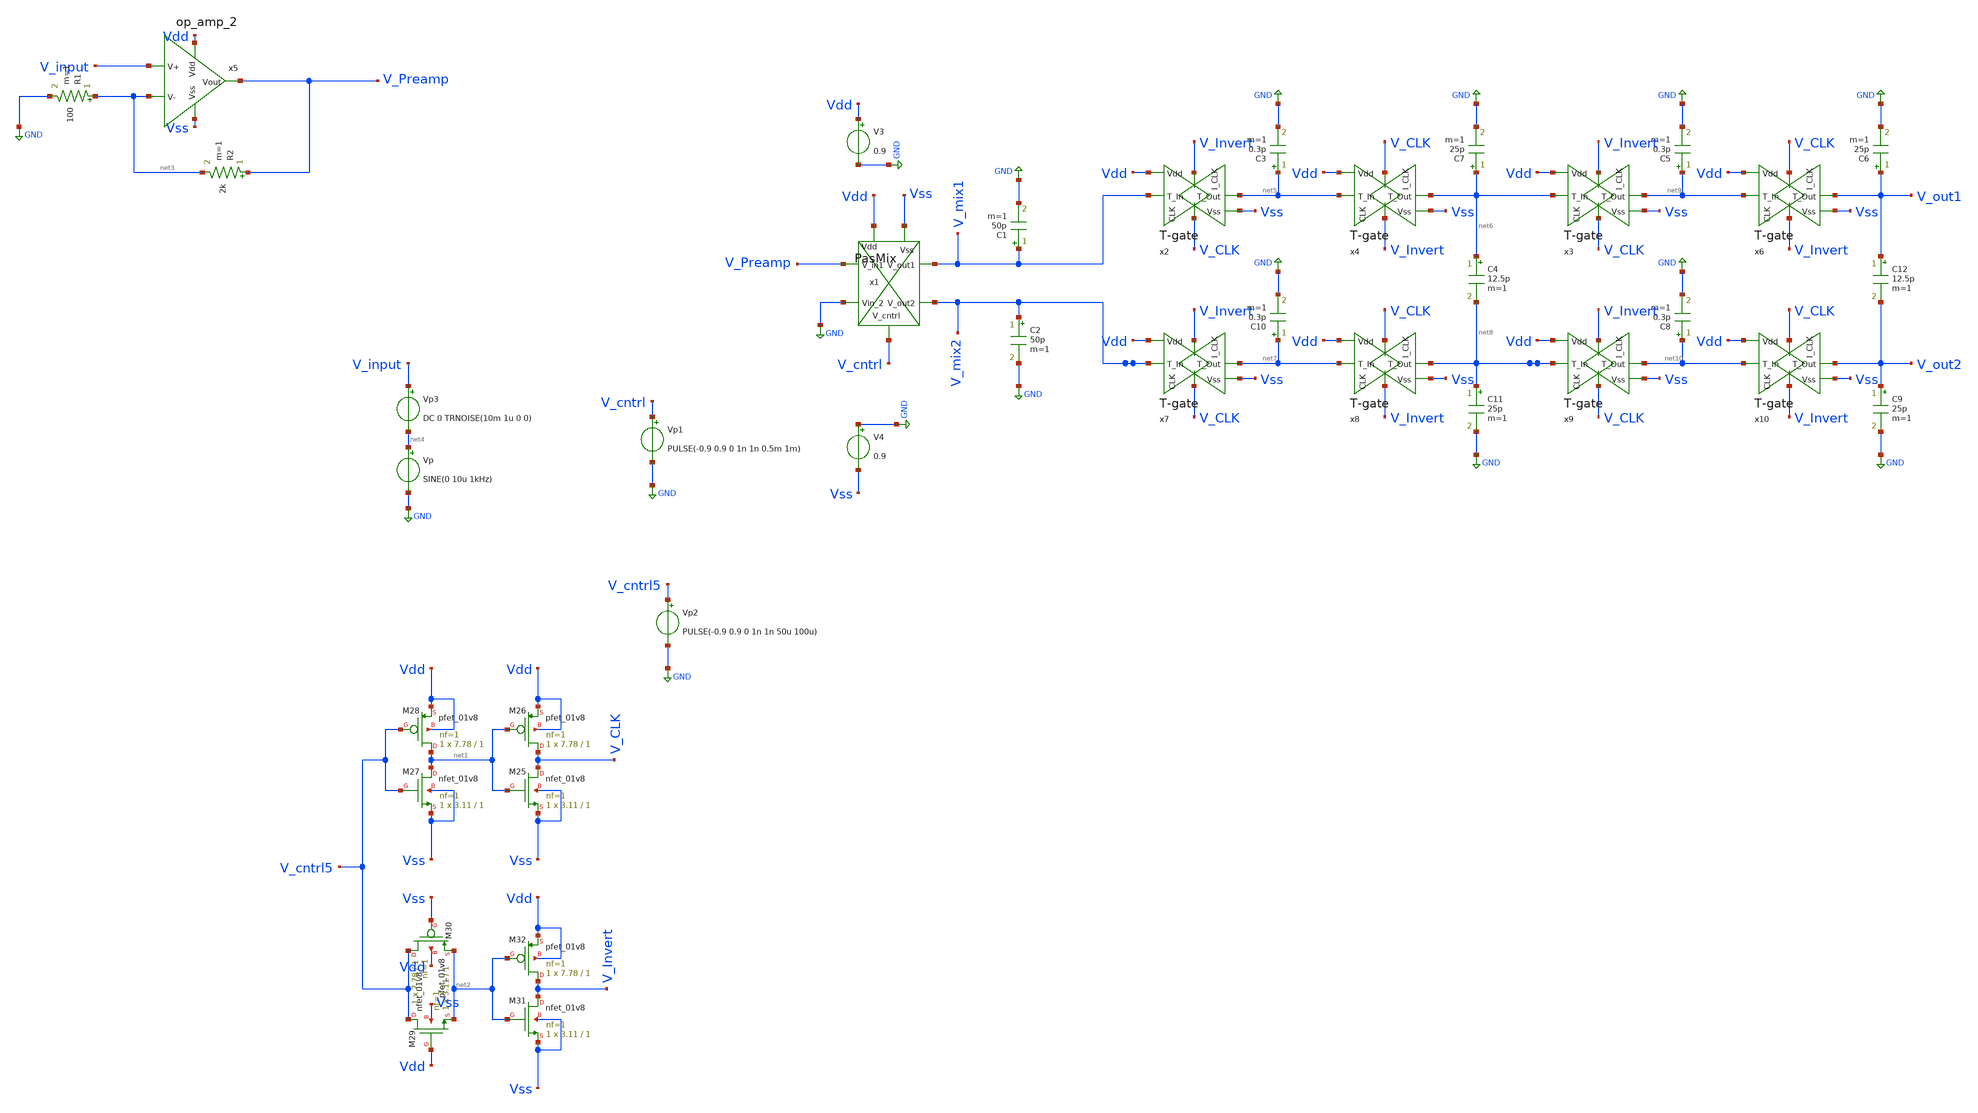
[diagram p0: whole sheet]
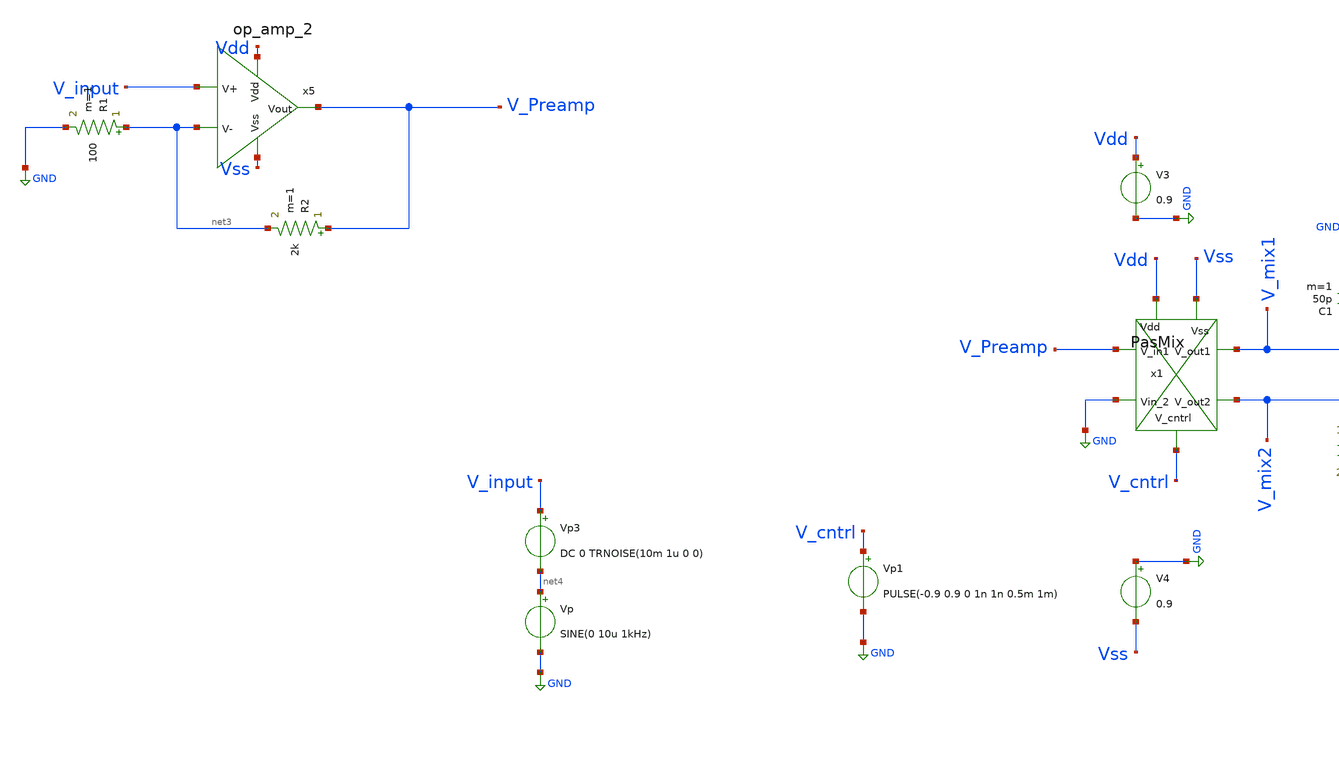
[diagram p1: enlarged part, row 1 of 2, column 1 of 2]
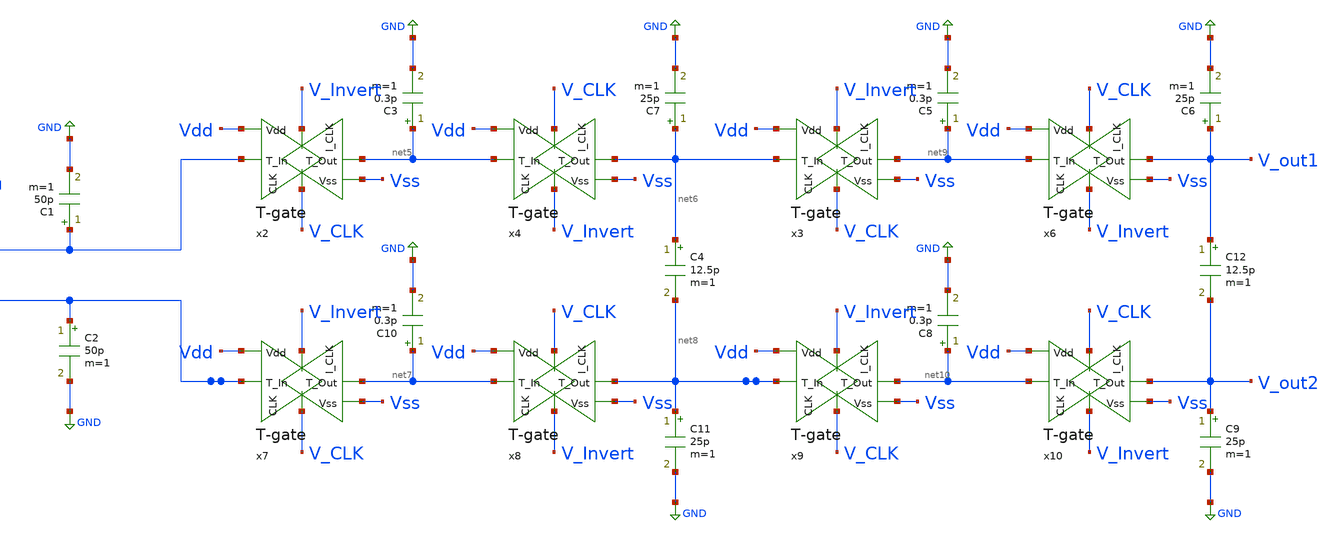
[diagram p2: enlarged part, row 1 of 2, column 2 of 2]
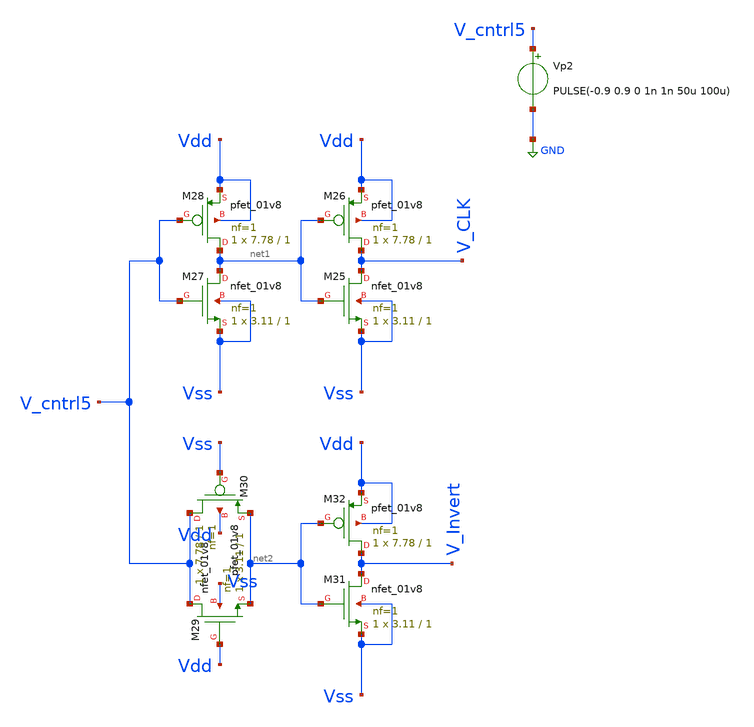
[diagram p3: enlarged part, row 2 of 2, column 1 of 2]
** sch_path: xschem/Mixer2.sch
**.subckt Mixer2
V3 Vdd GND 0.9
V4 GND Vss 0.9
Vp net4 GND SINE(0 10u 1kHz)
Vp1 V_cntrl GND PULSE(-0.9 0.9 0 1n 1n 0.5m 1m)
C2 V_mix2 GND 50p m=1
XM25 V_CLK net1 Vss Vss sky130_fd_pr__nfet_01v8 L=1 W=3.11 nf=1 ad='int((1 + 1)/2) * 3.11 / 1 * 0.29'
+ as='int((1 + 2)/2) * 3.11 / 1 * 0.29' pd='2*int((1 + 1)/2) * (3.11 / 1 + 0.29)' ps='2*int((1 + 2)/2) * (3.11 / 1 + 0.29)'
+ nrd='0.29 / 3.11 ' nrs='0.29 / 3.11 ' sa=0 sb=0 sd=0 mult=1 m=1
XM26 V_CLK net1 Vdd Vdd sky130_fd_pr__pfet_01v8 L=1 W=7.78 nf=1 ad='int((1 + 1)/2) * 7.78 / 1 * 0.29'
+ as='int((1 + 2)/2) * 7.78 / 1 * 0.29' pd='2*int((1 + 1)/2) * (7.78 / 1 + 0.29)' ps='2*int((1 + 2)/2) * (7.78 / 1 + 0.29)'
+ nrd='0.29 / 7.78 ' nrs='0.29 / 7.78 ' sa=0 sb=0 sd=0 mult=1 m=1
XM27 net1 V_cntrl5 Vss Vss sky130_fd_pr__nfet_01v8 L=1 W=3.11 nf=1 ad='int((1 + 1)/2) * 3.11 / 1 * 0.29'
+ as='int((1 + 2)/2) * 3.11 / 1 * 0.29' pd='2*int((1 + 1)/2) * (3.11 / 1 + 0.29)' ps='2*int((1 + 2)/2) * (3.11 / 1 + 0.29)'
+ nrd='0.29 / 3.11 ' nrs='0.29 / 3.11 ' sa=0 sb=0 sd=0 mult=1 m=1
XM28 net1 V_cntrl5 Vdd Vdd sky130_fd_pr__pfet_01v8 L=1 W=7.78 nf=1 ad='int((1 + 1)/2) * 7.78 / 1 * 0.29'
+ as='int((1 + 2)/2) * 7.78 / 1 * 0.29' pd='2*int((1 + 1)/2) * (7.78 / 1 + 0.29)' ps='2*int((1 + 2)/2) * (7.78 / 1 + 0.29)'
+ nrd='0.29 / 7.78 ' nrs='0.29 / 7.78 ' sa=0 sb=0 sd=0 mult=1 m=1
XM29 V_cntrl5 Vdd net2 Vss sky130_fd_pr__nfet_01v8 L=1 W=3.11 nf=1 ad='int((1 + 1)/2) * 3.11 / 1 * 0.29'
+ as='int((1 + 2)/2) * 3.11 / 1 * 0.29' pd='2*int((1 + 1)/2) * (3.11 / 1 + 0.29)' ps='2*int((1 + 2)/2) * (3.11 / 1 + 0.29)'
+ nrd='0.29 / 3.11 ' nrs='0.29 / 3.11 ' sa=0 sb=0 sd=0 mult=1 m=1
XM30 V_cntrl5 Vss net2 Vdd sky130_fd_pr__pfet_01v8 L=1 W=7.78 nf=1 ad='int((1 + 1)/2) * 7.78 / 1 * 0.29'
+ as='int((1 + 2)/2) * 7.78 / 1 * 0.29' pd='2*int((1 + 1)/2) * (7.78 / 1 + 0.29)' ps='2*int((1 + 2)/2) * (7.78 / 1 + 0.29)'
+ nrd='0.29 / 7.78 ' nrs='0.29 / 7.78 ' sa=0 sb=0 sd=0 mult=1 m=1
XM31 V_Invert net2 Vss Vss sky130_fd_pr__nfet_01v8 L=1 W=3.11 nf=1 ad='int((1 + 1)/2) * 3.11 / 1 * 0.29'
+ as='int((1 + 2)/2) * 3.11 / 1 * 0.29' pd='2*int((1 + 1)/2) * (3.11 / 1 + 0.29)' ps='2*int((1 + 2)/2) * (3.11 / 1 + 0.29)'
+ nrd='0.29 / 3.11 ' nrs='0.29 / 3.11 ' sa=0 sb=0 sd=0 mult=1 m=1
XM32 V_Invert net2 Vdd Vdd sky130_fd_pr__pfet_01v8 L=1 W=7.78 nf=1 ad='int((1 + 1)/2) * 7.78 / 1 * 0.29'
+ as='int((1 + 2)/2) * 7.78 / 1 * 0.29' pd='2*int((1 + 1)/2) * (7.78 / 1 + 0.29)' ps='2*int((1 + 2)/2) * (7.78 / 1 + 0.29)'
+ nrd='0.29 / 7.78 ' nrs='0.29 / 7.78 ' sa=0 sb=0 sd=0 mult=1 m=1
Vp2 V_cntrl5 GND PULSE(-0.9 0.9 0 1n 1n 50u 100u)
x1 Vdd V_cntrl Vss V_mix1 V_Preamp V_mix2 GND PasMix
C1 V_mix1 GND 50p m=1
x5 Vdd V_Preamp V_input net3 Vss op_amp_2
R1 net3 GND 100 m=1
R2 V_Preamp net3 2k m=1
x2 V_Invert V_mix1 net5 Vdd Vss V_CLK T-gate
C3 net5 GND 0.3p m=1
x4 V_CLK net5 net6 Vdd Vss V_Invert T-gate
C7 net6 GND 25p m=1
x7 V_Invert V_mix2 net7 Vdd Vss V_CLK T-gate
C10 net7 GND 0.3p m=1
x8 V_CLK net7 net8 Vdd Vss V_Invert T-gate
C11 net8 GND 25p m=1
C4 net6 net8 12.5p m=1
x3 V_Invert net6 net9 Vdd Vss V_CLK T-gate
C5 net9 GND 0.3p m=1
x6 V_CLK net9 V_out1 Vdd Vss V_Invert T-gate
C6 V_out1 GND 25p m=1
x9 V_Invert net8 net10 Vdd Vss V_CLK T-gate
C8 net10 GND 0.3p m=1
x10 V_CLK net10 V_out2 Vdd Vss V_Invert T-gate
C9 V_out2 GND 25p m=1
C12 V_out1 V_out2 12.5p m=1
Vp3 V_input net4 DC 0 TRNOISE(10m 1u 0 0)
**** begin user architecture code


.lib /foss/pdks/sky130A/libs.tech/combined/sky130.lib.spice tt
.control
 tran 1u 100m

 plot v(v_input)
 plot v(V_CLK) v(V_Invert)
 plot v(V_Preamp)

 plot (v(V_out1)-v(V_out2))
 *plot v(V_out)


 plot (v(V_mix1)-v(V_mix2))
 *plot (v(C_1) - v(C_2))
 *plot v(V_mix1) v(V_out2)
 *noise v(V_out2) Vp dec 10 1 1MEG
 *fourier 1kHz v(V_Preamp) (v(V_mix1)-v(V_out2)) (v(V_out1)-v(V_out2))
 *plot fourier13[1] vs fourier13[0]
 *plot fourier12[1] vs fourier12[0]
 *plot fourier11[1] vs fourier11[0]
.endc
.end

**** end user architecture code
**.ends

* expanding   symbol:  PasMix.sym # of pins=7
** sym_path: xschem/PasMix.sym
** sch_path: xschem/PasMix.sch
.subckt PasMix Vdd V_cntrl Vss V_out1 V_in1 V_out2 Vin_2
*.ipin V_in1
*.ipin Vin_2
*.opin V_out1
*.opin V_out2
*.ipin Vdd
*.ipin Vss
*.ipin V_cntrl
x1 V_Invert V_in1 V_out1 Vdd Vss V_CLK T-gate
x2 V_Invert Vin_2 V_out2 Vdd Vss V_CLK T-gate
x3 V_CLK Vin_2 V_out1 Vdd Vss V_Invert T-gate
x4 V_CLK V_in1 V_out2 Vdd Vss V_Invert T-gate
XM3 net1 V_cntrl Vss Vss sky130_fd_pr__nfet_g5v0d10v5 L=1 W=1 nf=1 ad='int((1 + 1)/2) * 1 / 1 * 0.29'
+ as='int((1 + 2)/2) * 1 / 1 * 0.29' pd='2*int((1 + 1)/2) * (1 / 1 + 0.29)' ps='2*int((1 + 2)/2) * (1 / 1 + 0.29)'
+ nrd='0.29 / 1 ' nrs='0.29 / 1 ' sa=0 sb=0 sd=0 mult=1 m=1
XM4 net1 V_cntrl Vdd Vdd sky130_fd_pr__pfet_g5v0d10v5 L=1 W=3 nf=1 ad='int((1 + 1)/2) * 3 / 1 * 0.29'
+ as='int((1 + 2)/2) * 3 / 1 * 0.29' pd='2*int((1 + 1)/2) * (3 / 1 + 0.29)' ps='2*int((1 + 2)/2) * (3 / 1 + 0.29)'
+ nrd='0.29 / 3 ' nrs='0.29 / 3 ' sa=0 sb=0 sd=0 mult=1 m=1
XM5 V_CLK net1 Vss Vss sky130_fd_pr__nfet_g5v0d10v5 L=1 W=3 nf=1 ad='int((1 + 1)/2) * 3 / 1 * 0.29' as='int((1 + 2)/2) * 3 / 1 * 0.29'
+ pd='2*int((1 + 1)/2) * (3 / 1 + 0.29)' ps='2*int((1 + 2)/2) * (3 / 1 + 0.29)' nrd='0.29 / 3 ' nrs='0.29 / 3 '
+ sa=0 sb=0 sd=0 mult=1 m=1
XM6 V_CLK net1 Vdd Vdd sky130_fd_pr__pfet_g5v0d10v5 L=1 W=27 nf=1 ad='int((1 + 1)/2) * 27 / 1 * 0.29'
+ as='int((1 + 2)/2) * 27 / 1 * 0.29' pd='2*int((1 + 1)/2) * (27 / 1 + 0.29)' ps='2*int((1 + 2)/2) * (27 / 1 + 0.29)'
+ nrd='0.29 / 27 ' nrs='0.29 / 27 ' sa=0 sb=0 sd=0 mult=1 m=1
XM7 net2 net1 Vss Vss sky130_fd_pr__nfet_g5v0d10v5 L=1 W=3 nf=1 ad='int((1 + 1)/2) * 3 / 1 * 0.29' as='int((1 + 2)/2) * 3 / 1 * 0.29'
+ pd='2*int((1 + 1)/2) * (3 / 1 + 0.29)' ps='2*int((1 + 2)/2) * (3 / 1 + 0.29)' nrd='0.29 / 3 ' nrs='0.29 / 3 '
+ sa=0 sb=0 sd=0 mult=1 m=1
XM8 net2 net1 Vdd Vdd sky130_fd_pr__pfet_g5v0d10v5 L=1 W=27 nf=1 ad='int((1 + 1)/2) * 27 / 1 * 0.29'
+ as='int((1 + 2)/2) * 27 / 1 * 0.29' pd='2*int((1 + 1)/2) * (27 / 1 + 0.29)' ps='2*int((1 + 2)/2) * (27 / 1 + 0.29)'
+ nrd='0.29 / 27 ' nrs='0.29 / 27 ' sa=0 sb=0 sd=0 mult=1 m=1
XM9 V_Invert net2 Vss Vss sky130_fd_pr__nfet_g5v0d10v5 L=1 W=3 nf=1 ad='int((1 + 1)/2) * 3 / 1 * 0.29'
+ as='int((1 + 2)/2) * 3 / 1 * 0.29' pd='2*int((1 + 1)/2) * (3 / 1 + 0.29)' ps='2*int((1 + 2)/2) * (3 / 1 + 0.29)'
+ nrd='0.29 / 3 ' nrs='0.29 / 3 ' sa=0 sb=0 sd=0 mult=1 m=1
XM10 V_Invert net2 Vdd Vdd sky130_fd_pr__pfet_g5v0d10v5 L=1 W=27 nf=1 ad='int((1 + 1)/2) * 27 / 1 * 0.29'
+ as='int((1 + 2)/2) * 27 / 1 * 0.29' pd='2*int((1 + 1)/2) * (27 / 1 + 0.29)' ps='2*int((1 + 2)/2) * (27 / 1 + 0.29)'
+ nrd='0.29 / 27 ' nrs='0.29 / 27 ' sa=0 sb=0 sd=0 mult=1 m=1
.ends


* expanding   symbol:  op_amp_2.sym # of pins=5
** sym_path: xschem/op_amp_2.sym
** sch_path: xschem/op_amp_2.sch
.subckt op_amp_2 Vdd Vout V+ V- Vss
*.opin Vout
*.ipin Vdd
*.ipin Vss
*.ipin V+
*.ipin V-
XM1 net1 net1 Vss Vss sky130_fd_pr__nfet_01v8 L=1 W=9.35 nf=1 ad='int((1 + 1)/2) * 9.35 / 1 * 0.29' as='int((1 + 2)/2) * 9.35 / 1 * 0.29'
+ pd='2*int((1 + 1)/2) * (9.35 / 1 + 0.29)' ps='2*int((1 + 2)/2) * (9.35 / 1 + 0.29)' nrd='0.29 / 9.35 '
+ nrs='0.29 / 9.35 ' sa=0 sb=0 sd=0 mult=1 m=1
XM3 net2 net1 Vss Vss sky130_fd_pr__nfet_01v8 L=1 W=9.35 nf=1 ad='int((1 + 1)/2) * 9.35 / 1 * 0.29' as='int((1 + 2)/2) * 9.35 / 1 * 0.29'
+ pd='2*int((1 + 1)/2) * (9.35 / 1 + 0.29)' ps='2*int((1 + 2)/2) * (9.35 / 1 + 0.29)' nrd='0.29 / 9.35 '
+ nrs='0.29 / 9.35 ' sa=0 sb=0 sd=0 mult=1 m=1
XM10 net3 V- net2 Vss sky130_fd_pr__nfet_01v8 L=1 W=3.11 nf=1 ad='int((1 + 1)/2) * 3.11 / 1 * 0.29' as='int((1 + 2)/2) * 3.11 / 1 * 0.29'
+ pd='2*int((1 + 1)/2) * (3.11 / 1 + 0.29)' ps='2*int((1 + 2)/2) * (3.11 / 1 + 0.29)' nrd='0.29 / 3.11 '
+ nrs='0.29 / 3.11 ' sa=0 sb=0 sd=0 mult=1 m=1
XM11 net4 V+ net2 Vss sky130_fd_pr__nfet_01v8 L=1 W=3.11 nf=1 ad='int((1 + 1)/2) * 3.11 / 1 * 0.29' as='int((1 + 2)/2) * 3.11 / 1 * 0.29'
+ pd='2*int((1 + 1)/2) * (3.11 / 1 + 0.29)' ps='2*int((1 + 2)/2) * (3.11 / 1 + 0.29)' nrd='0.29 / 3.11 '
+ nrs='0.29 / 3.11 ' sa=0 sb=0 sd=0 mult=1 m=1
XM5 net4 net3 Vdd Vdd sky130_fd_pr__pfet_01v8 L=1 W=3.41 nf=1 ad='int((1 + 1)/2) * 3.41 / 1 * 0.29' as='int((1 + 2)/2) * 3.41 / 1 * 0.29'
+ pd='2*int((1 + 1)/2) * (3.41 / 1 + 0.29)' ps='2*int((1 + 2)/2) * (3.41 / 1 + 0.29)' nrd='0.29 / 3.41 '
+ nrs='0.29 / 3.41 ' sa=0 sb=0 sd=0 mult=1 m=1
XM6 net3 net3 Vdd Vdd sky130_fd_pr__pfet_01v8 L=1 W=3.41 nf=1 ad='int((1 + 1)/2) * 3.41 / 1 * 0.29' as='int((1 + 2)/2) * 3.41 / 1 * 0.29'
+ pd='2*int((1 + 1)/2) * (3.41 / 1 + 0.29)' ps='2*int((1 + 2)/2) * (3.41 / 1 + 0.29)' nrd='0.29 / 3.41 '
+ nrs='0.29 / 3.41 ' sa=0 sb=0 sd=0 mult=1 m=1
C1 Vout net4 500f m=1
C2 GND Vout 2p m=1
XM2 net1 net1 Vdd Vdd sky130_fd_pr__pfet_01v8 L=1 W=8.92 nf=1 ad='int((1 + 1)/2) * 8.92 / 1 * 0.29' as='int((1 + 2)/2) * 8.92 / 1 * 0.29'
+ pd='2*int((1 + 1)/2) * (8.92 / 1 + 0.29)' ps='2*int((1 + 2)/2) * (8.92 / 1 + 0.29)' nrd='0.29 / 8.92 '
+ nrs='0.29 / 8.92 ' sa=0 sb=0 sd=0 mult=1 m=1
XM7 Vout net4 Vdd Vdd sky130_fd_pr__pfet_01v8 L=1 W=54.48 nf=1 ad='int((1 + 1)/2) * 54.48 / 1 * 0.29'
+ as='int((1 + 2)/2) * 54.48 / 1 * 0.29' pd='2*int((1 + 1)/2) * (54.48 / 1 + 0.29)' ps='2*int((1 + 2)/2) * (54.48 / 1 + 0.29)'
+ nrd='0.29 / 54.48 ' nrs='0.29 / 54.48 ' sa=0 sb=0 sd=0 mult=1 m=1
XM9 Vout net1 Vss Vss sky130_fd_pr__nfet_01v8 L=1 W=74.77 nf=1 ad='int((1 + 1)/2) * 74.77 / 1 * 0.29'
+ as='int((1 + 2)/2) * 74.77 / 1 * 0.29' pd='2*int((1 + 1)/2) * (74.77 / 1 + 0.29)' ps='2*int((1 + 2)/2) * (74.77 / 1 + 0.29)'
+ nrd='0.29 / 74.77 ' nrs='0.29 / 74.77 ' sa=0 sb=0 sd=0 mult=1 m=1
.ends


* expanding   symbol:  T-gate.sym # of pins=6
** sym_path: xschem/T-gate.sym
** sch_path: xschem/T-gate.sch
.subckt T-gate I_CLK T_In T_Out Vdd Vss CLK
*.ipin T_In
*.opin T_Out
*.ipin Vdd
*.ipin Vss
*.ipin I_CLK
*.ipin CLK
XM1 T_In I_CLK T_Out Vdd sky130_fd_pr__pfet_g5v0d10v5 L=0.5 W=3 nf=1 ad='int((1 + 1)/2) * 3 / 1 * 0.29'
+ as='int((1 + 2)/2) * 3 / 1 * 0.29' pd='2*int((1 + 1)/2) * (3 / 1 + 0.29)' ps='2*int((1 + 2)/2) * (3 / 1 + 0.29)'
+ nrd='0.29 / 3 ' nrs='0.29 / 3 ' sa=0 sb=0 sd=0 mult=1 m=1
XM3 T_Out CLK T_In Vss sky130_fd_pr__nfet_g5v0d10v5 L=0.5 W=1 nf=1 ad='int((1 + 1)/2) * 1 / 1 * 0.29'
+ as='int((1 + 2)/2) * 1 / 1 * 0.29' pd='2*int((1 + 1)/2) * (1 / 1 + 0.29)' ps='2*int((1 + 2)/2) * (1 / 1 + 0.29)'
+ nrd='0.29 / 1 ' nrs='0.29 / 1 ' sa=0 sb=0 sd=0 mult=1 m=1
XM2 T_Out CLK T_Out Vdd sky130_fd_pr__pfet_g5v0d10v5 L=0.5 W=1.5 nf=1 ad='int((1 + 1)/2) * 1.5 / 1 * 0.29'
+ as='int((1 + 2)/2) * 1.5 / 1 * 0.29' pd='2*int((1 + 1)/2) * (1.5 / 1 + 0.29)' ps='2*int((1 + 2)/2) * (1.5 / 1 + 0.29)'
+ nrd='0.29 / 1.5 ' nrs='0.29 / 1.5 ' sa=0 sb=0 sd=0 mult=1 m=1
XM4 T_In CLK T_In Vdd sky130_fd_pr__pfet_g5v0d10v5 L=0.5 W=1.5 nf=1 ad='int((1 + 1)/2) * 1.5 / 1 * 0.29'
+ as='int((1 + 2)/2) * 1.5 / 1 * 0.29' pd='2*int((1 + 1)/2) * (1.5 / 1 + 0.29)' ps='2*int((1 + 2)/2) * (1.5 / 1 + 0.29)'
+ nrd='0.29 / 1.5 ' nrs='0.29 / 1.5 ' sa=0 sb=0 sd=0 mult=1 m=1
XM5 T_In I_CLK T_In Vss sky130_fd_pr__nfet_g5v0d10v5 L=0.5 W=0.5 nf=1 ad='int((1 + 1)/2) * 0.5 / 1 * 0.29'
+ as='int((1 + 2)/2) * 0.5 / 1 * 0.29' pd='2*int((1 + 1)/2) * (0.5 / 1 + 0.29)' ps='2*int((1 + 2)/2) * (0.5 / 1 + 0.29)'
+ nrd='0.29 / 0.5 ' nrs='0.29 / 0.5 ' sa=0 sb=0 sd=0 mult=1 m=1
XM6 T_Out I_CLK T_Out Vss sky130_fd_pr__nfet_g5v0d10v5 L=0.5 W=0.5 nf=1 ad='int((1 + 1)/2) * 0.5 / 1 * 0.29'
+ as='int((1 + 2)/2) * 0.5 / 1 * 0.29' pd='2*int((1 + 1)/2) * (0.5 / 1 + 0.29)' ps='2*int((1 + 2)/2) * (0.5 / 1 + 0.29)'
+ nrd='0.29 / 0.5 ' nrs='0.29 / 0.5 ' sa=0 sb=0 sd=0 mult=1 m=1
.ends

.GLOBAL GND
.end
